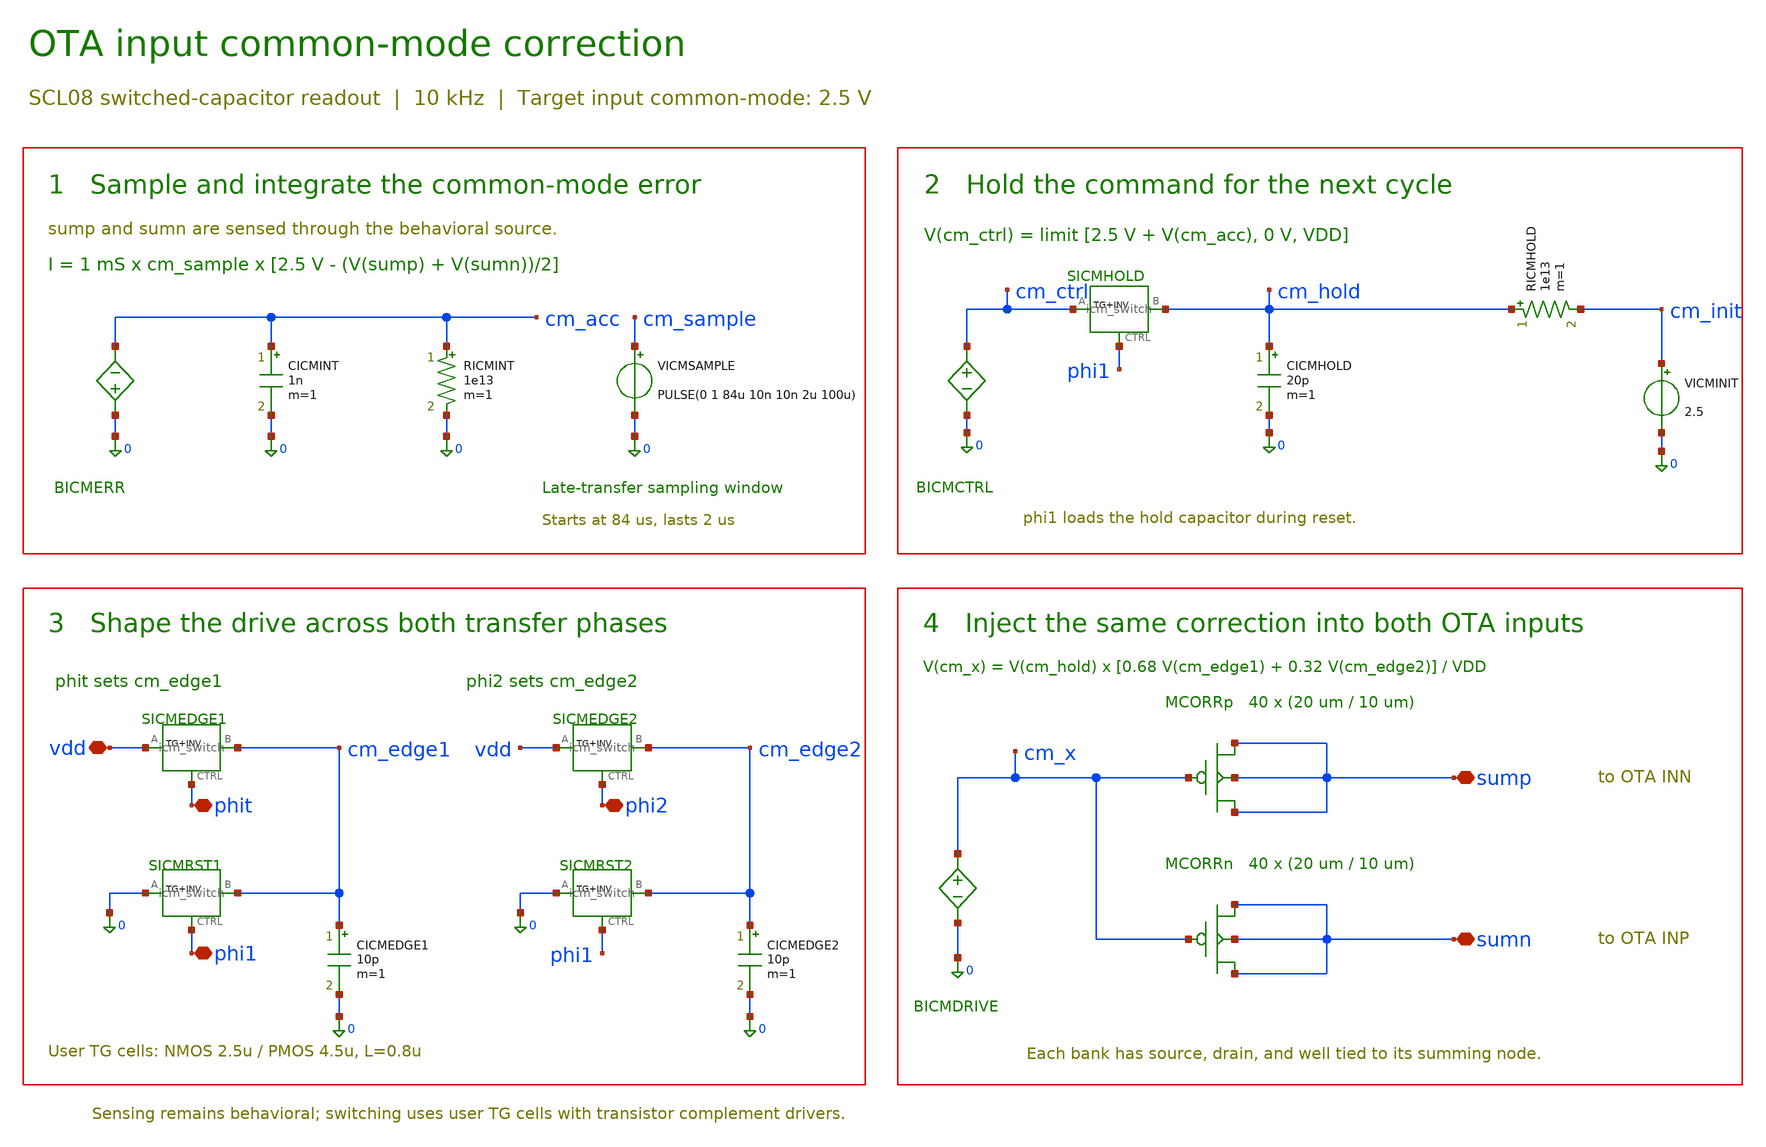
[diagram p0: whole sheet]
** sch_path: Mixed_Signal/Integrated_Design/symbols/ota_input_cm_servo.sch
**.subckt ota_input_cm_servo vdd phit phi1 phi2 sump sumn
*.iopin vdd
*.iopin phit
*.iopin phi1
*.iopin phi2
*.iopin sump
*.iopin sumn
BICMERR 0 cm_acc I = 1m*v(cm_sample)*(2.5-(v(sump)+v(sumn))/2)
CICMINT cm_acc 0 1n m=1
RICMINT cm_acc 0 1e13 m=1
VICMSAMPLE cm_sample 0 PULSE(0 1 84u 10n 10n 2u 100u)
BICMCTRL cm_ctrl 0 V = max(0,min(v(vdd),2.5+v(cm_acc)))
XSICMHOLD cm_ctrl cm_hold phi1 vdd user_tg_control
CICMHOLD cm_hold 0 20p m=1
RICMHOLD cm_hold cm_init 1e13 m=1
VICMINIT cm_init 0 2.5
XSICMEDGE1 vdd cm_edge1 phit vdd user_tg_control
XSICMRST1 0 cm_edge1 phi1 vdd user_tg_control
CICMEDGE1 cm_edge1 0 10p m=1
XSICMEDGE2 vdd cm_edge2 phi2 vdd user_tg_control
XSICMRST2 0 cm_edge2 phi1 vdd user_tg_control
CICMEDGE2 cm_edge2 0 10p m=1
BICMDRIVE cm_x 0 V = ((.68*v(cm_edge1)+.32*v(cm_edge2))/max(.1,v(vdd)))*v(cm_hold)
MCORRp sump cm_x sump sump P W=20u L=10u M=40 AD=90p AS=90p PD=49u PS=49u
MCORRn sumn cm_x sumn sumn P W=20u L=10u M=40 AD=90p AS=90p PD=49u PS=49u
**** begin user architecture code
.model icm_hold SW(Ron=10 Roff=1e14 Vt=2 Vh=.1)
.model icm_edge_set SW(Ron=3000 Roff=1e13 Vt=1 Vh=.05)
.model icm_edge_reset SW(Ron=100k Roff=1e13 Vt=2 Vh=.1)
**** end user architecture code
**.ends
.end
